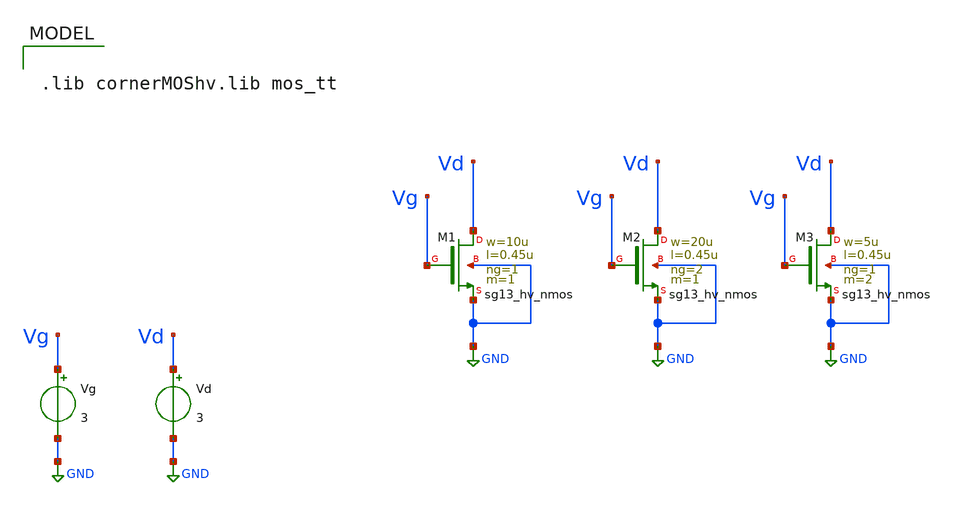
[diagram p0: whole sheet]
** sch_path: xschem/top/untitled-1.sch
**.subckt untitled-1
XM1 Vd Vg GND GND sg13_hv_nmos w=10u l=0.45u ng=1 m=1 mm_ok=1
XM2 Vd Vg GND GND sg13_hv_nmos w=20u l=0.45u ng=2 m=1 mm_ok=1
XM3 Vd Vg GND GND sg13_hv_nmos w=5u l=0.45u ng=1 m=2 mm_ok=1
Vg Vg GND 3
Vd Vd GND 3
**** begin user architecture code



.control
save all  @n.xm1.nsg13_hv_nmos[vds]  @n.xm1.nsg13_hv_nmos[ids]  @n.xm2.nsg13_hv_nmos[vds]
+  @n.xm2.nsg13_hv_nmos[ids]  @n.xm3.nsg13_hv_nmos[vds]  @n.xm3.nsg13_hv_nmos[ids]

dc Vd 0 3.3 0.01 Vg 0 3.3 0.66

let vds1 = @n.xm1.nsg13_hv_nmos[vds]
let ids1 = @n.xm1.nsg13_hv_nmos[ids]

let vds2 = @n.xm2.nsg13_hv_nmos[vds]
let ids2 = @n.xm2.nsg13_hv_nmos[ids]

let vds3 = @n.xm3.nsg13_hv_nmos[vds]
let ids3 = @n.xm3.nsg13_hv_nmos[ids]

plot ids1 vs vds1
.endc



.lib cornerMOShv.lib mos_tt

**** end user architecture code
**.ends
.GLOBAL GND
.end
